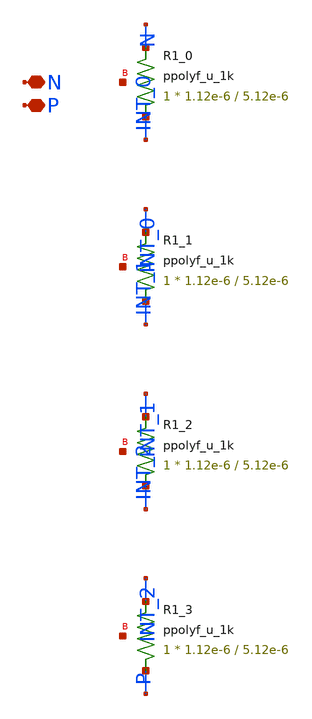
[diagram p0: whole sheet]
** sch_path: design/LELO_TR_GF180MCUD/LELOTR_RES4.sch
**.subckt LELOTR_RES4 N P
*.iopin N
*.iopin P
XR1_0 INT_0 N net1 ppolyf_u_1k r_width=1.12e-6 r_length=5.12e-6 m=1
XR1_1 INT_1 INT_0 net2 ppolyf_u_1k r_width=1.12e-6 r_length=5.12e-6 m=1
XR1_2 INT_2 INT_1 net3 ppolyf_u_1k r_width=1.12e-6 r_length=5.12e-6 m=1
XR1_3 P INT_2 net4 ppolyf_u_1k r_width=1.12e-6 r_length=5.12e-6 m=1
**.ends
.end
